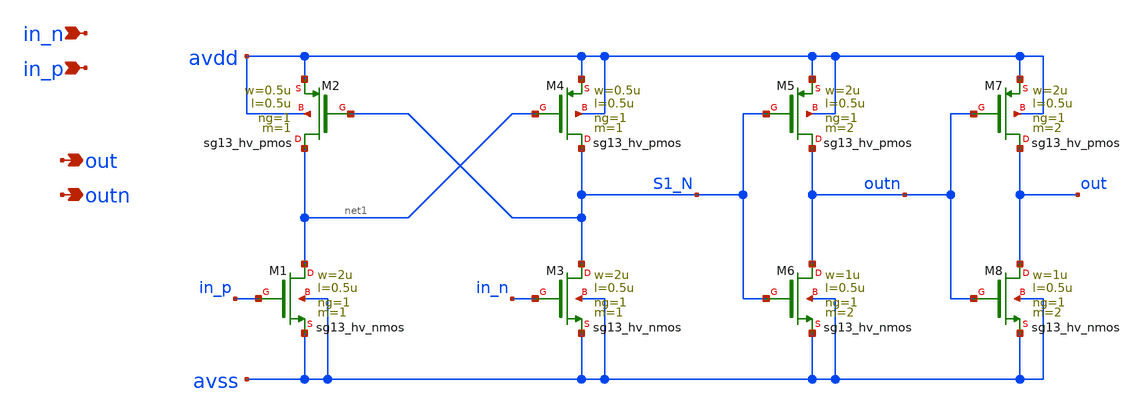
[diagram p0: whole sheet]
** sch_path: macros/ocd_analog_switches/schematic/xschem/sw_lvl_shift.sch
**.subckt sw_lvl_shift in_n in_p out outn
*.ipin in_n
*.ipin in_p
*.opin out
*.opin outn
XM1 net1 in_p avss avss sg13_hv_nmos w=2u l=0.5u ng=1 m=1 mm_ok=1
XM2 net1 S1_N avdd avdd sg13_hv_pmos w=0.5u l=0.5u ng=1 m=1 mm_ok=1
XM3 S1_N in_n avss avss sg13_hv_nmos w=2u l=0.5u ng=1 m=1 mm_ok=1
XM4 S1_N net1 avdd avdd sg13_hv_pmos w=0.5u l=0.5u ng=1 m=1 mm_ok=1
XM5 outn S1_N avdd avdd sg13_hv_pmos w=2u l=0.5u ng=1 m=2 mm_ok=1
XM6 outn S1_N avss avss sg13_hv_nmos w=1u l=0.5u ng=1 m=2 mm_ok=1
XM7 out outn avdd avdd sg13_hv_pmos w=2u l=0.5u ng=1 m=2 mm_ok=1
XM8 out outn avss avss sg13_hv_nmos w=1u l=0.5u ng=1 m=2 mm_ok=1
**.ends
.end
